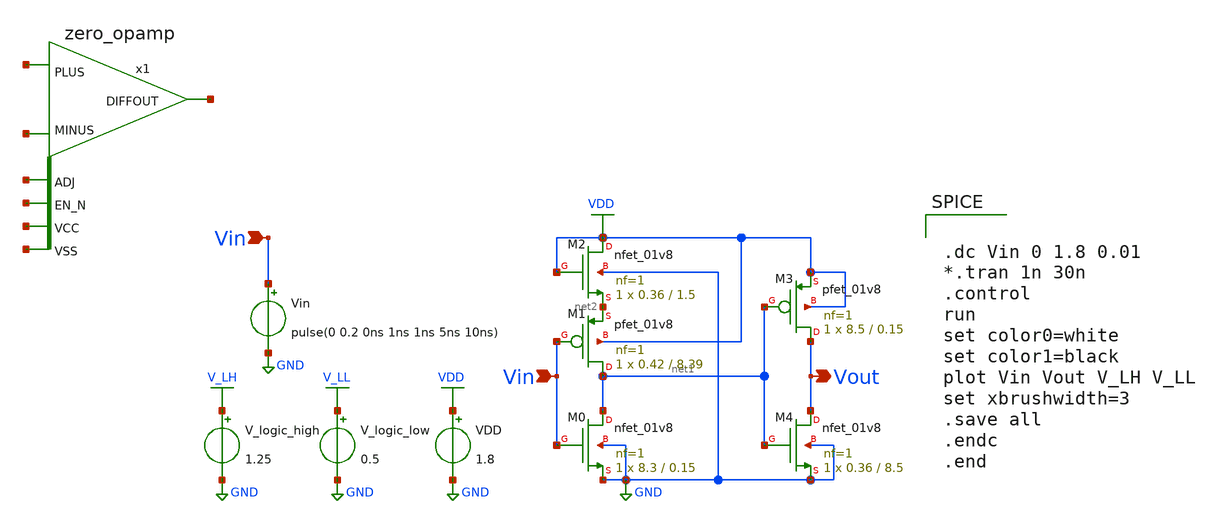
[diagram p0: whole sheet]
** sch_path: xschem/Vth_sch/th02_1.sch
* StefanSchippers/xschem_sky130/sky130_tests/zero_opamp.sch:
* Copyright 2021 Stefan Frederik Schippers
* Licensed under the Apache License, Version 2.0 (the "License");
**.subckt th02_1 Vin Vin Vout
*.ipin Vin
*.ipin Vin
*.opin Vout
VDD VDD GND 1.8
Vin Vin GND pulse(0 0.2 0ns 1ns 1ns 5ns 10ns)
V_logic_high V_LH GND 1.25
V_logic_low V_LL GND 0.5
XM3 Vout net1 VDD VDD sky130_fd_pr__pfet_01v8 L=0.15 W=8.5 nf=1 ad='int((nf+1)/2) * W/nf * 0.29' as='int((nf+2)/2) * W/nf * 0.29'
+ pd='2*int((nf+1)/2) * (W/nf + 0.29)' ps='2*int((nf+2)/2) * (W/nf + 0.29)' nrd='0.29 / W' nrs='0.29 / W'
+ sa=0 sb=0 sd=0 mult=1 m=1
XM4 Vout net1 GND GND sky130_fd_pr__nfet_01v8 L=8.5 W=0.36 nf=1 ad='int((nf+1)/2) * W/nf * 0.29' as='int((nf+2)/2) * W/nf * 0.29'
+ pd='2*int((nf+1)/2) * (W/nf + 0.29)' ps='2*int((nf+2)/2) * (W/nf + 0.29)' nrd='0.29 / W' nrs='0.29 / W'
+ sa=0 sb=0 sd=0 mult=1 m=1
XM1 net1 Vin net2 VDD sky130_fd_pr__pfet_01v8 L=8.39 W=0.42 nf=1 ad='int((nf+1)/2) * W/nf * 0.29' as='int((nf+2)/2) * W/nf * 0.29'
+ pd='2*int((nf+1)/2) * (W/nf + 0.29)' ps='2*int((nf+2)/2) * (W/nf + 0.29)' nrd='0.29 / W' nrs='0.29 / W'
+ sa=0 sb=0 sd=0 mult=1 m=1
XM0 net1 Vin GND GND sky130_fd_pr__nfet_01v8 L=0.15 W=8.3 nf=1 ad='int((nf+1)/2) * W/nf * 0.29' as='int((nf+2)/2) * W/nf * 0.29'
+ pd='2*int((nf+1)/2) * (W/nf + 0.29)' ps='2*int((nf+2)/2) * (W/nf + 0.29)' nrd='0.29 / W' nrs='0.29 / W'
+ sa=0 sb=0 sd=0 mult=1 m=1
XM2 VDD VDD net2 GND sky130_fd_pr__nfet_01v8 L=1.5 W=0.36 nf=1 ad='int((nf+1)/2) * W/nf * 0.29' as='int((nf+2)/2) * W/nf * 0.29'
+ pd='2*int((nf+1)/2) * (W/nf + 0.29)' ps='2*int((nf+2)/2) * (W/nf + 0.29)' nrd='0.29 / W' nrs='0.29 / W'
+ sa=0 sb=0 sd=0 mult=1 m=1
x1 net3 net4 net5 net6 net7 net8 net9 zero_opamp
**** begin user architecture code


.lib /usr/local/share/pdk/sky130A/libs.tech/ngspice/sky130.lib.spice tt

.save all





.dc Vin 0 1.8 0.01
*.tran 1n 30n
.control
run
set color0=white
set color1=black
plot Vin Vout V_LH V_LL
set xbrushwidth=3
.save all
.endc
.end


**** end user architecture code
**.ends

* expanding   symbol:  sky130_tests/zero_opamp.sym # of pins=7
** sym_path: sky130_tests/zero_opamp.sym
** sch_path: sky130_tests/zero_opamp.sch
.subckt zero_opamp EN_N MINUS PLUS DIFFOUT VCC VSS ADJ
*.ipin PLUS
*.ipin MINUS
*.ipin EN_N
*.ipin VSS
*.ipin VCC
*.opin DIFFOUT
*.ipin ADJ
C6 G1 0 2f m=1
XM4 net9 EN_N VCC VCC sky130_fd_pr__pfet_01v8 L=8 W=2 nf=1 ad='W * 0.29' as='W * 0.29' pd='W + 2 * 0.29'
+ ps='W + 2 * 0.29' nrd=0 nrs=0 sa=0 sb=0 sd=0 mult=1 m=1
XM18 G2 G2 net7 VSS sky130_fd_pr__nfet_01v8_lvt L=4 W=2 nf=1 ad='W * 0.29' as='W * 0.29' pd='2*(W + 0.29)'
+ ps='2*(W + 0.29)' nrd=0 nrs=0 sa=0 sb=0 sd=0 mult=1 m=1
XM2 G1 G1 net8 VSS sky130_fd_pr__nfet_01v8_lvt L=4 W=2 nf=1 ad='W * 0.29' as='W * 0.29' pd='2*(W + 0.29)'
+ ps='2*(W + 0.29)' nrd=0 nrs=0 sa=0 sb=0 sd=0 mult=1 m=1
XMR G2 PLUS net10 VCC sky130_fd_pr__pfet_01v8_lvt L=2 W=8 nf=1 ad='W * 0.29' as='W * 0.29' pd='2*(W + 0.29)'
+ ps='2*(W + 0.29)' nrd=0 nrs=0 sa=0 sb=0 sd=0 mult=1 m=1
XML G1 MINUS net11 VCC sky130_fd_pr__pfet_01v8_lvt L=2 W=8 nf=1 ad='W * 0.29' as='W * 0.29' pd='2*(W + 0.29)'
+ ps='2*(W + 0.29)' nrd=0 nrs=0 sa=0 sb=0 sd=0 mult=1 m=1
v1 SP net11 0
.save i(v1)
C4 SP 0 2f m=1
C1 G2 0 2f m=1
C5 DIFFOUT 0 4f m=1
XM6 DIFFOUT G2 net1 VSS sky130_fd_pr__nfet_01v8_lvt L=4 W=2 nf=1 ad='W * 0.29' as='W * 0.29' pd='2*(W + 0.29)'
+ ps='2*(W + 0.29)' nrd=0 nrs=0 sa=0 sb=0 sd=0 mult=1 m=1
v2 SP net10 0
.save i(v2)
v4 net1 VSS 0
.save i(v4)
v6 net9 SP 0
.save i(v6)
XM7 DIFFOUT EN_N VSS VSS sky130_fd_pr__nfet_01v8 L=0.15 W=0.5 nf=1 ad='W * 0.29' as='W * 0.29' pd='2*(W + 0.29)'
+ ps='2*(W + 0.29)' nrd=0 nrs=0 sa=0 sb=0 sd=0 mult=1 m=1
XM46 net12 EN_N VCC VCC sky130_fd_pr__pfet_01v8 L=0.15 W=5 nf=1 ad='W * 0.29' as='W * 0.29' pd='W + 2 * 0.29'
+ ps='W + 2 * 0.29' nrd=0 nrs=0 sa=0 sb=0 sd=0 mult=1 m=1
v17 net12 net3 0
.save i(v17)
XM12 net2 G1 VSS VSS sky130_fd_pr__nfet_01v8_lvt L=4 W=2 nf=1 ad='W * 0.29' as='W * 0.29' pd='2*(W + 0.29)'
+ ps='2*(W + 0.29)' nrd=0 nrs=0 sa=0 sb=0 sd=0 mult=1 m=1
XM54 net2 net2 net3 VCC sky130_fd_pr__pfet_01v8_lvt L=4 W=4 nf=1 ad='W * 0.29' as='W * 0.29' pd='2*(W + 0.29)'
+ ps='2*(W + 0.29)' nrd=0 nrs=0 sa=0 sb=0 sd=0 mult=1 m=1
XM5 DIFFOUT net2 net3 VCC sky130_fd_pr__pfet_01v8_lvt L=4 W=4 nf=1 ad='W * 0.29' as='W * 0.29' pd='2*(W + 0.29)'
+ ps='2*(W + 0.29)' nrd=0 nrs=0 sa=0 sb=0 sd=0 mult=1 m=1
XM8 net5 ADJ net4 VCC sky130_fd_pr__pfet_01v8_lvt L=1 W=1 nf=1 ad='W * 0.29' as='W * 0.29' pd='W + 2 * 0.29'
+ ps='W + 2 * 0.29' nrd=0 nrs=0 sa=0 sb=0 sd=0 mult=1 m=1
XM9 net5 ADJ net6 VSS sky130_fd_pr__nfet_01v8 L=1 W=0.5 nf=1 ad='W * 0.29' as='W * 0.29' pd='W + 2 * 0.29'
+ ps='W + 2 * 0.29' nrd=0 nrs=0 sa=0 sb=0 sd=0 mult=1 m=1
XM10 net6 VCC VSS VSS sky130_fd_pr__nfet_01v8 L=8 W=0.5 nf=1 ad='W * 0.29' as='W * 0.29' pd='2*(W + 0.29)'
+ ps='2*(W + 0.29)' nrd=0 nrs=0 sa=0 sb=0 sd=0 mult=1 m=1
XM1 net4 EN_N VCC VCC sky130_fd_pr__pfet_01v8 L=8 W=1 nf=1 ad='W * 0.29' as='W * 0.29' pd='W + 2 * 0.29'
+ ps='W + 2 * 0.29' nrd=0 nrs=0 sa=0 sb=0 sd=0 mult=1 m=1
v3 net5 G1 0
.save i(v3)
v5 net7 VSS 0
.save i(v5)
v7 net8 VSS 0
.save i(v7)
.ends

.GLOBAL VDD
.GLOBAL GND
.GLOBAL V_LH
.GLOBAL V_LL
.end
